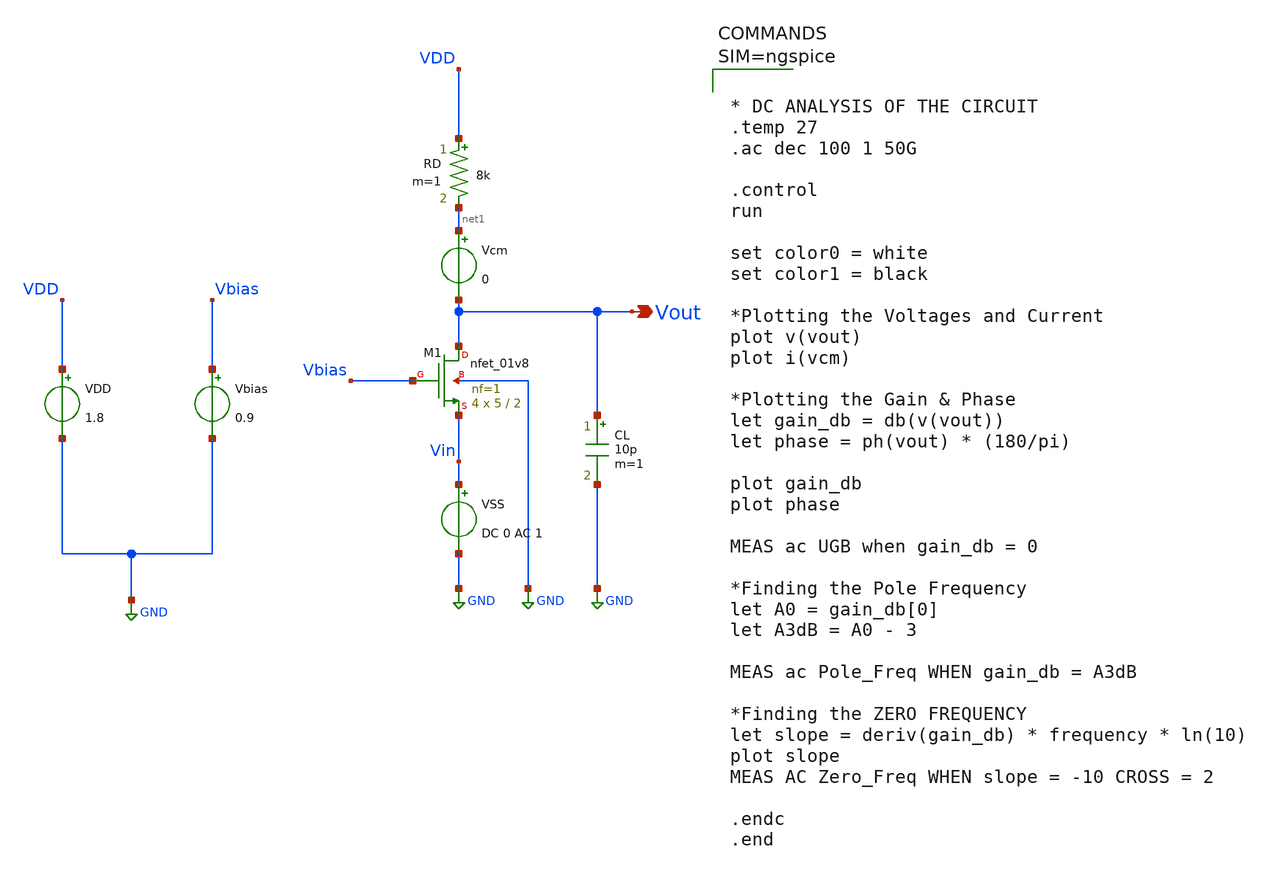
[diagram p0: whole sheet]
** sch_path: Common_Gate_MOS_Amps/Common_Gate_Amp_AC_Analysis.sch
**.subckt Common_Gate_Amp_AC_Analysis Vout
*.opin Vout
XM1 Vout Vbias Vin GND sky130_fd_pr__nfet_01v8 L=2 W=5 nf=1 ad='int((1 + 1)/2) * 5 / 1 * 0.29' as='int((1 + 2)/2) * 5 / 1 * 0.29'
+ pd='2*int((1 + 1)/2) * (5 / 1 + 0.29)' ps='2*int((1 + 2)/2) * (5 / 1 + 0.29)' nrd='0.29 / 5 ' nrs='0.29 / 5 '
+ sa=0 sb=0 sd=0 mult=4 m=4
RD VDD net1 8k m=1
CL Vout GND 10p m=1
VDD VDD GND 1.8
Vbias Vbias GND 0.9
VSS Vin GND DC 0 AC 1
Vcm net1 Vout 0
**** begin user architecture code

** opencircuitdesign pdks install
.lib $::SKYWATER_MODELS/sky130.lib.spice tt




* DC ANALYSIS OF THE CIRCUIT
.temp 27
.ac dec 100 1 50G

.control
run

set color0 = white
set color1 = black

*Plotting the Voltages and Current
plot v(vout)
plot i(vcm)

*Plotting the Gain & Phase
let gain_db = db(v(vout))
let phase = ph(vout) * (180/pi)

plot gain_db
plot phase

MEAS ac UGB when gain_db = 0

*Finding the Pole Frequency
let A0 = gain_db[0]
let A3dB = A0 - 3

MEAS ac Pole_Freq WHEN gain_db = A3dB

*Finding the ZERO FREQUENCY
let slope = deriv(gain_db) * frequency * ln(10)
plot slope
MEAS AC Zero_Freq WHEN slope = -10 CROSS = 2

.endc
.end




**** end user architecture code
**.ends
.GLOBAL GND
.end
